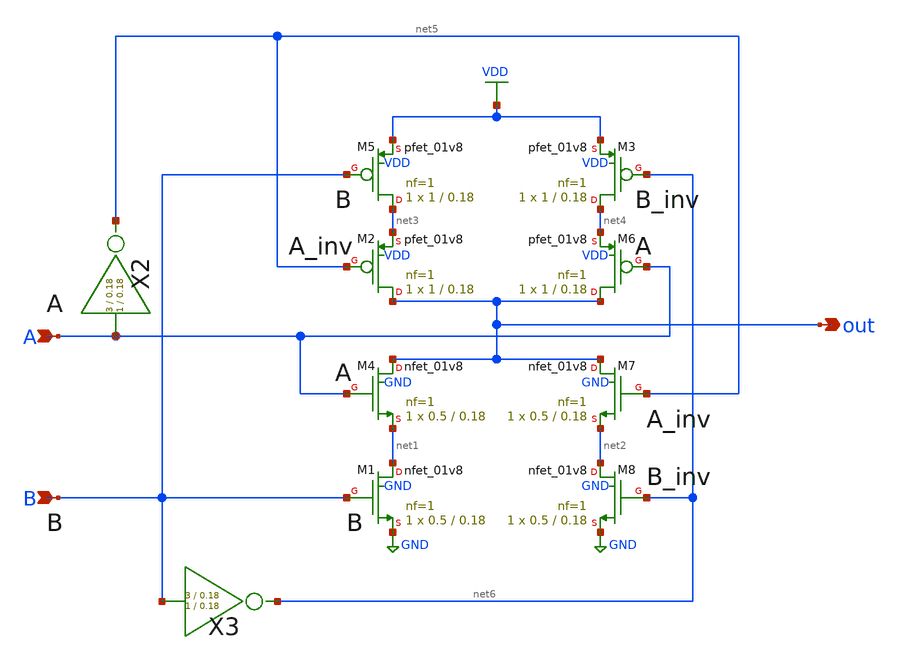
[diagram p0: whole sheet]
** sch_path: xschem/exor_gate/exor_gate.sch
**.subckt exor_gate A B out
*.ipin A
*.ipin B
*.opin out
XM4 out A net1 GND sky130_fd_pr__nfet_01v8 L=0.18 W=0.5 nf=1 ad='int((nf+1)/2) * W/nf * 0.29' as='int((nf+2)/2) * W/nf * 0.29'
+ pd='2*int((nf+1)/2) * (W/nf + 0.29)' ps='2*int((nf+2)/2) * (W/nf + 0.29)' nrd='0.29 / W' nrs='0.29 / W'
+ sa=0 sb=0 sd=0 mult=1 m=1
XM5 net3 B VDD VDD sky130_fd_pr__pfet_01v8 L=0.18 W=1 nf=1 ad='int((nf+1)/2) * W/nf * 0.29' as='int((nf+2)/2) * W/nf * 0.29'
+ pd='2*int((nf+1)/2) * (W/nf + 0.29)' ps='2*int((nf+2)/2) * (W/nf + 0.29)' nrd='0.29 / W' nrs='0.29 / W'
+ sa=0 sb=0 sd=0 mult=1 m=1
XM1 net1 B GND GND sky130_fd_pr__nfet_01v8 L=0.18 W=0.5 nf=1 ad='int((nf+1)/2) * W/nf * 0.29' as='int((nf+2)/2) * W/nf * 0.29'
+ pd='2*int((nf+1)/2) * (W/nf + 0.29)' ps='2*int((nf+2)/2) * (W/nf + 0.29)' nrd='0.29 / W' nrs='0.29 / W'
+ sa=0 sb=0 sd=0 mult=1 m=1
XM2 out net5 net3 VDD sky130_fd_pr__pfet_01v8 L=0.18 W=1 nf=1 ad='int((nf+1)/2) * W/nf * 0.29' as='int((nf+2)/2) * W/nf * 0.29'
+ pd='2*int((nf+1)/2) * (W/nf + 0.29)' ps='2*int((nf+2)/2) * (W/nf + 0.29)' nrd='0.29 / W' nrs='0.29 / W'
+ sa=0 sb=0 sd=0 mult=1 m=1
XM3 net4 net6 VDD VDD sky130_fd_pr__pfet_01v8 L=0.18 W=1 nf=1 ad='int((nf+1)/2) * W/nf * 0.29' as='int((nf+2)/2) * W/nf * 0.29'
+ pd='2*int((nf+1)/2) * (W/nf + 0.29)' ps='2*int((nf+2)/2) * (W/nf + 0.29)' nrd='0.29 / W' nrs='0.29 / W'
+ sa=0 sb=0 sd=0 mult=1 m=1
XM6 out A net4 VDD sky130_fd_pr__pfet_01v8 L=0.18 W=1 nf=1 ad='int((nf+1)/2) * W/nf * 0.29' as='int((nf+2)/2) * W/nf * 0.29'
+ pd='2*int((nf+1)/2) * (W/nf + 0.29)' ps='2*int((nf+2)/2) * (W/nf + 0.29)' nrd='0.29 / W' nrs='0.29 / W'
+ sa=0 sb=0 sd=0 mult=1 m=1
XM7 out net5 net2 GND sky130_fd_pr__nfet_01v8 L=0.18 W=0.5 nf=1 ad='int((nf+1)/2) * W/nf * 0.29' as='int((nf+2)/2) * W/nf * 0.29'
+ pd='2*int((nf+1)/2) * (W/nf + 0.29)' ps='2*int((nf+2)/2) * (W/nf + 0.29)' nrd='0.29 / W' nrs='0.29 / W'
+ sa=0 sb=0 sd=0 mult=1 m=1
XM8 net2 net6 GND GND sky130_fd_pr__nfet_01v8 L=0.18 W=0.5 nf=1 ad='int((nf+1)/2) * W/nf * 0.29' as='int((nf+2)/2) * W/nf * 0.29'
+ pd='2*int((nf+1)/2) * (W/nf + 0.29)' ps='2*int((nf+2)/2) * (W/nf + 0.29)' nrd='0.29 / W' nrs='0.29 / W'
+ sa=0 sb=0 sd=0 mult=1 m=1
X3 B net6 inv Wpmos=3 Lpmos=0.18 Wnmos=1 Lnmos=0.18
X2 A net5 inv Wpmos=3 Lpmos=0.18 Wnmos=1 Lnmos=0.18
**.ends

* expanding   symbol:  inv/inv.sym # of pins=2
** sym_path: xschem/inv/inv.sym
** sch_path: xschem/inv/inv.sch
.subckt inv in out  Wpmos=3 Lpmos=0.18 Wnmos=1 Lnmos=0.18
*.ipin in
*.iopin out
XM1 out in GND GND sky130_fd_pr__nfet_01v8 L=Lnmos W=Wnmos nf=1 ad='int((nf+1)/2) * W/nf * 0.29' as='int((nf+2)/2) * W/nf * 0.29'
+ pd='2*int((nf+1)/2) * (W/nf + 0.29)' ps='2*int((nf+2)/2) * (W/nf + 0.29)' nrd='0.29 / W' nrs='0.29 / W'
+ sa=0 sb=0 sd=0 mult=1 m=1
XM2 out in VDD VDD sky130_fd_pr__pfet_01v8 L=Lpmos W=Wpmos nf=1 ad='int((nf+1)/2) * W/nf * 0.29' as='int((nf+2)/2) * W/nf * 0.29'
+ pd='2*int((nf+1)/2) * (W/nf + 0.29)' ps='2*int((nf+2)/2) * (W/nf + 0.29)' nrd='0.29 / W' nrs='0.29 / W'
+ sa=0 sb=0 sd=0 mult=1 m=1
.ends

.GLOBAL VDD
.GLOBAL GND
.end
